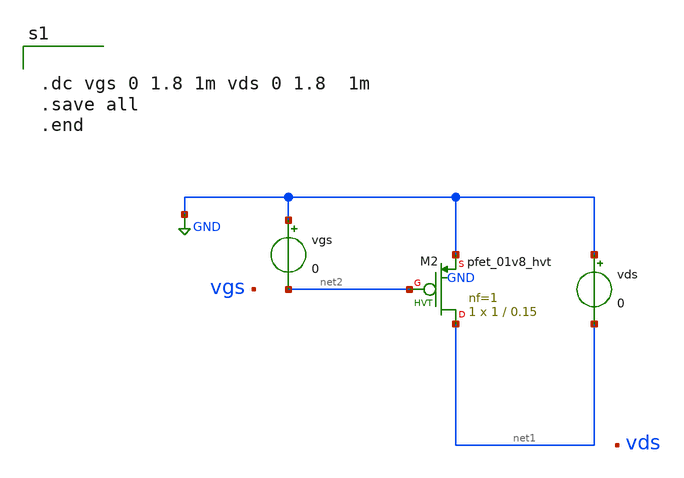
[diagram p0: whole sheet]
** sch_path: xschem/Polarizzazione.sch
**.subckt Polarizzazione
XM2 net1 net2 GND GND sky130_fd_pr__pfet_01v8_hvt L=0.15 W=1 nf=1 ad='int((nf+1)/2) * W/nf * 0.29' as='int((nf+2)/2) * W/nf * 0.29'
+ pd='2*int((nf+1)/2) * (W/nf + 0.29)' ps='2*int((nf+2)/2) * (W/nf + 0.29)' nrd='0.29 / W' nrs='0.29 / W'
+ sa=0 sb=0 sd=0 mult=1 m=1
vgs GND net2 0
vds GND net1 0
**** begin user architecture code


.dc vgs 0 1.8 1m vds 0 1.8  1m
.save all
.end



** opencircuitdesign pdks install
.lib $::SKYWATER_MODELS/sky130.lib.spice tt


**** end user architecture code
**.ends
.GLOBAL GND
.end
